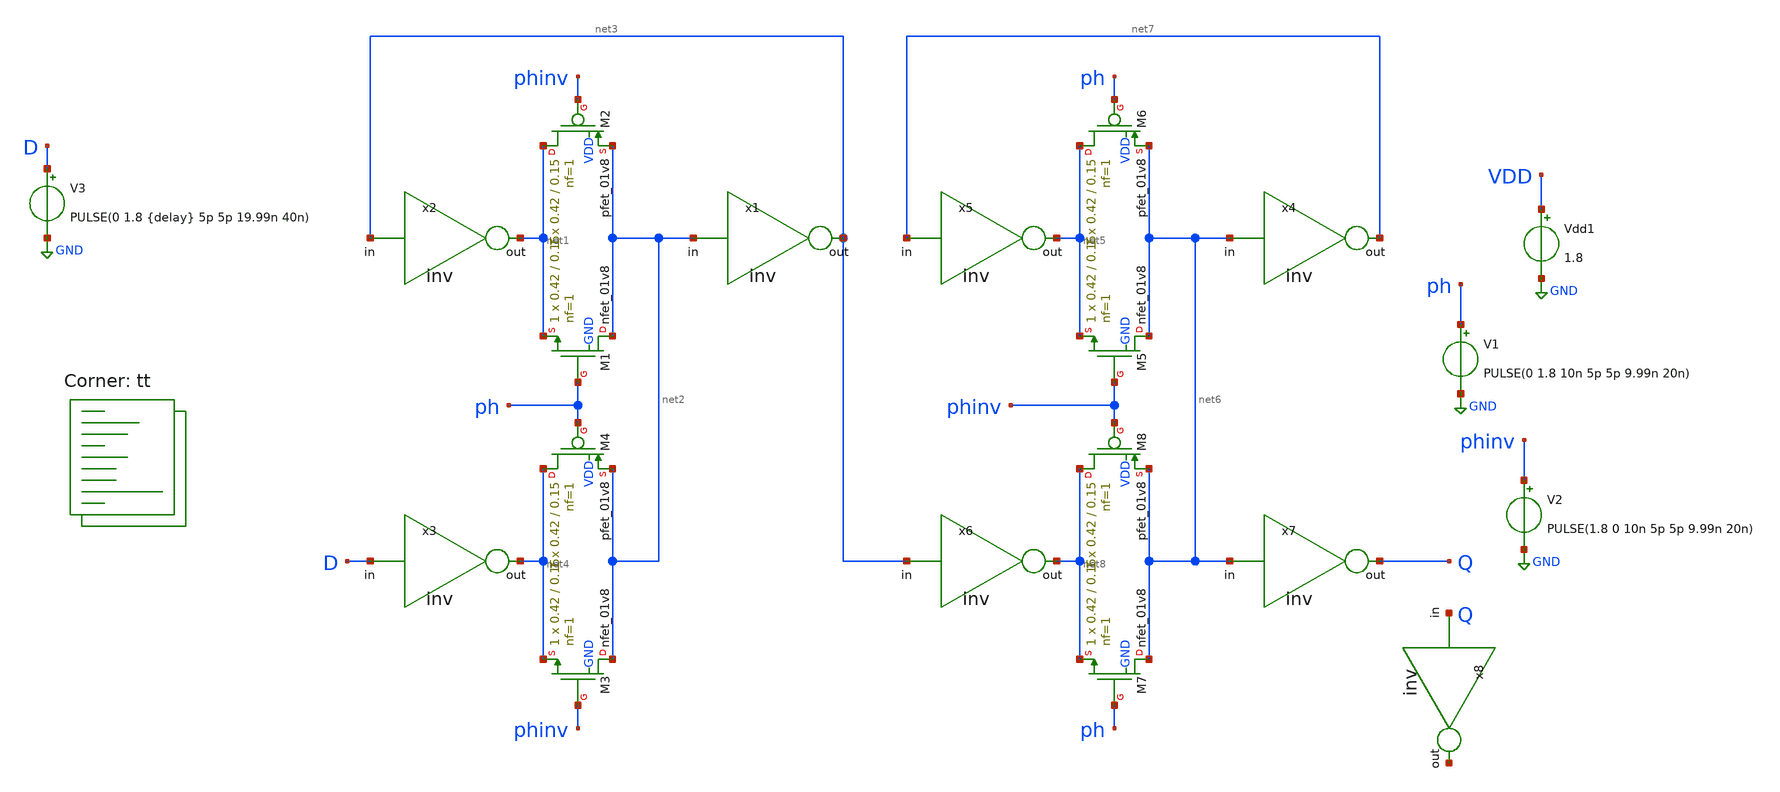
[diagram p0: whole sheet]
** sch_path: tutorial_5/tutorial_5.sch
**.subckt tutorial_5
V3 D GND PULSE(0 1.8 {delay} 5p 5p 19.99n 40n)
XM1 net2 ph net1 GND sky130_fd_pr__nfet_01v8 L=0.15 W=0.42 nf=1 ad='int((nf+1)/2) * W/nf * 0.29' as='int((nf+2)/2) * W/nf * 0.29'
+ pd='2*int((nf+1)/2) * (W/nf + 0.29)' ps='2*int((nf+2)/2) * (W/nf + 0.29)' nrd='0.29 / W' nrs='0.29 / W'
+ sa=0 sb=0 sd=0 mult=1 m=1
XM2 net1 phinv net2 VDD sky130_fd_pr__pfet_01v8 L=0.15 W=0.42 nf=1 ad='int((nf+1)/2) * W/nf * 0.29' as='int((nf+2)/2) * W/nf * 0.29'
+ pd='2*int((nf+1)/2) * (W/nf + 0.29)' ps='2*int((nf+2)/2) * (W/nf + 0.29)' nrd='0.29 / W' nrs='0.29 / W'
+ sa=0 sb=0 sd=0 mult=1 m=1
x1 net3 net2 inv
x2 net1 net3 inv
XM3 net2 phinv net4 GND sky130_fd_pr__nfet_01v8 L=0.15 W=0.42 nf=1 ad='int((nf+1)/2) * W/nf * 0.29' as='int((nf+2)/2) * W/nf * 0.29'
+ pd='2*int((nf+1)/2) * (W/nf + 0.29)' ps='2*int((nf+2)/2) * (W/nf + 0.29)' nrd='0.29 / W' nrs='0.29 / W'
+ sa=0 sb=0 sd=0 mult=1 m=1
XM4 net4 ph net2 VDD sky130_fd_pr__pfet_01v8 L=0.15 W=0.42 nf=1 ad='int((nf+1)/2) * W/nf * 0.29' as='int((nf+2)/2) * W/nf * 0.29'
+ pd='2*int((nf+1)/2) * (W/nf + 0.29)' ps='2*int((nf+2)/2) * (W/nf + 0.29)' nrd='0.29 / W' nrs='0.29 / W'
+ sa=0 sb=0 sd=0 mult=1 m=1
x3 net4 D inv
XM5 net6 phinv net5 GND sky130_fd_pr__nfet_01v8 L=0.15 W=0.42 nf=1 ad='int((nf+1)/2) * W/nf * 0.29' as='int((nf+2)/2) * W/nf * 0.29'
+ pd='2*int((nf+1)/2) * (W/nf + 0.29)' ps='2*int((nf+2)/2) * (W/nf + 0.29)' nrd='0.29 / W' nrs='0.29 / W'
+ sa=0 sb=0 sd=0 mult=1 m=1
XM6 net5 ph net6 VDD sky130_fd_pr__pfet_01v8 L=0.15 W=0.42 nf=1 ad='int((nf+1)/2) * W/nf * 0.29' as='int((nf+2)/2) * W/nf * 0.29'
+ pd='2*int((nf+1)/2) * (W/nf + 0.29)' ps='2*int((nf+2)/2) * (W/nf + 0.29)' nrd='0.29 / W' nrs='0.29 / W'
+ sa=0 sb=0 sd=0 mult=1 m=1
x4 net7 net6 inv
x5 net5 net7 inv
XM7 net6 ph net8 GND sky130_fd_pr__nfet_01v8 L=0.15 W=0.42 nf=1 ad='int((nf+1)/2) * W/nf * 0.29' as='int((nf+2)/2) * W/nf * 0.29'
+ pd='2*int((nf+1)/2) * (W/nf + 0.29)' ps='2*int((nf+2)/2) * (W/nf + 0.29)' nrd='0.29 / W' nrs='0.29 / W'
+ sa=0 sb=0 sd=0 mult=1 m=1
XM8 net8 phinv net6 VDD sky130_fd_pr__pfet_01v8 L=0.15 W=0.42 nf=1 ad='int((nf+1)/2) * W/nf * 0.29' as='int((nf+2)/2) * W/nf * 0.29'
+ pd='2*int((nf+1)/2) * (W/nf + 0.29)' ps='2*int((nf+2)/2) * (W/nf + 0.29)' nrd='0.29 / W' nrs='0.29 / W'
+ sa=0 sb=0 sd=0 mult=1 m=1
x6 net8 net3 inv
x7 Q net6 inv
V1 ph GND PULSE(0 1.8 10n 5p 5p 9.99n 20n)
V2 phinv GND PULSE(1.8 0 10n 5p 5p 9.99n 20n)
Vdd1 VDD GND 1.8
x8 net9 Q inv
**** begin user architecture code
.lib $::SKYWATER_MODELS/sky130.lib.spice tt


.param width_p = 0.84
.param delay = 9.80n
.control
let index = 1
let N = 60
set vcache = ( )
while index le N
   let newd = 9.80n + (index * 2p)
   alterparam delay = $&newd
   reset
   tran 2p 11n 9n
   set vcache = ( $vcache tran{$&index}.v(D) )
   set vcache = ( $vcache tran{$&index}.v(Q) )
   meas tran tdq trig v(D) val=0.9 rise=1 targ v(Q) val=0.9 rise=1
   meas tran tdp trig v(D) val=0.9 rise=1 targ v(ph) val=0.9 rise=1
   meas tran tpq trig v(ph) val=0.9 rise=1 targ v(Q) val=0.9 rise=1
   echo $&tdq $&tdp $&tpq >> rise.txt
   let index = index + 1
end
set vcache = ( $vcache v(ph) )
set nolegend
plot $vcache
let index = 61
let N = 120
set fcache = ( )
while index le N
   let newd = 9.80n + ((index - 60) * 2p)
   alterparam delay = $&newd
   reset
   tran 5p 31n 29n
   set fcache = ( $fcache tran{$&index}.v(D) )
   set fcache = ( $fcache tran{$&index}.v(Q) )
   meas tran tdq trig v(D) val=0.9 fall=1 targ v(Q) val=0.9 fall=1
   meas tran tdp trig v(D) val=0.9 fall=1 targ v(ph) val=0.9 rise=1
   meas tran tpq trig v(ph) val=0.9 rise=1 targ v(Q) val=0.9 fall=1
   echo $&tdq $&tdp $&tpq >> fall.txt
   let index = index + 1
end
set fcache = ( $fcache v(ph) )
set nolegend
plot $fcache
.endc


**** end user architecture code
**.ends

* expanding   symbol:  /home/EE23B038/ee5311/tutorial_5/inv.sym # of pins=2
** sym_path: tutorial_4/inv.sym
** sch_path: tutorial_4/inv.sch
.subckt inv out in
*.ipin in
*.opin out
XM1 out in GND GND sky130_fd_pr__nfet_01v8 L=0.15 W=0.42 nf=1 ad='int((nf+1)/2) * W/nf * 0.29' as='int((nf+2)/2) * W/nf * 0.29'
+ pd='2*int((nf+1)/2) * (W/nf + 0.29)' ps='2*int((nf+2)/2) * (W/nf + 0.29)' nrd='0.29 / W' nrs='0.29 / W'
+ sa=0 sb=0 sd=0 mult=1 m=1
XM2 out in VDD VDD sky130_fd_pr__pfet_01v8 L=0.15 W={width_p} nf=1 ad='int((nf+1)/2) * W/nf * 0.29' as='int((nf+2)/2) * W/nf * 0.29'
+ pd='2*int((nf+1)/2) * (W/nf + 0.29)' ps='2*int((nf+2)/2) * (W/nf + 0.29)' nrd='0.29 / W' nrs='0.29 / W'
+ sa=0 sb=0 sd=0 mult=1 m=1
.ends

.GLOBAL GND
.GLOBAL VDD
.end
